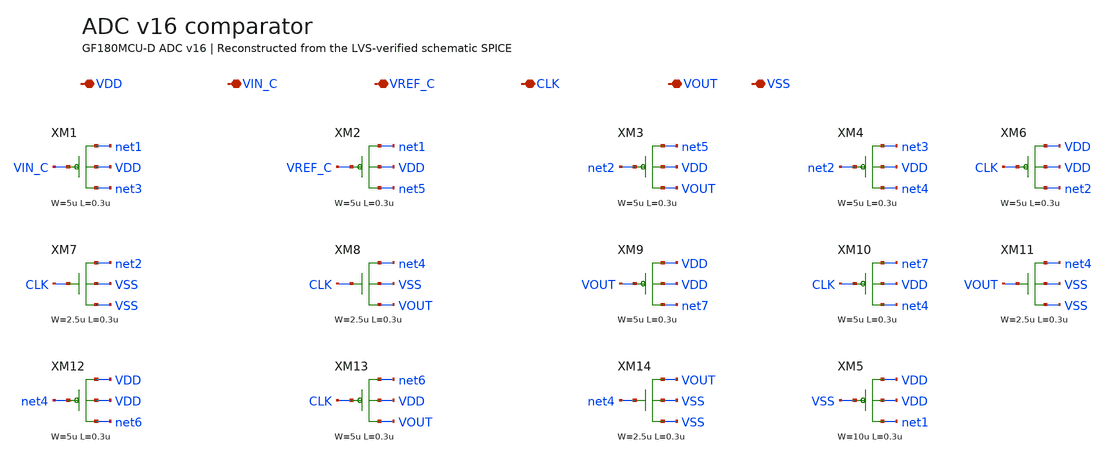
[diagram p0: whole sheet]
** sch_path: src/schematics/INTEGRATION/ADC_final/ADC_v17_Xschem/ADCv16_verified_comparator.sch
* Copyright (C) 1998-2026 Stefan Frederik Schippers
* This program is free software; you can redistribute it and/or modify
* it under the terms of the GNU General Public License as published by
* the Free Software Foundation; either version 2 of the License, or
* (at your option) any later version.
**.subckt ADCv16_verified_comparator VDD VIN_C VREF_C CLK VOUT VSS
*.iopin VDD
*.iopin VIN_C
*.iopin VREF_C
*.iopin CLK
*.iopin VOUT
*.iopin VSS
XM1 net3 VIN_C net1 VDD pfet_03v3 L=0.3u W=5u nf=1 ad='int((nf+1)/2) * W/nf * 0.18u' as='int((nf+2)/2) * W/nf * 0.18u'
+ pd='2*int((nf+1)/2) * (W/nf + 0.18u)' ps='2*int((nf+2)/2) * (W/nf + 0.18u)' nrd='0.18u / W' nrs='0.18u / W'
+ sa=0 sb=0 sd=0
XM2 net5 VREF_C net1 VDD pfet_03v3 L=0.3u W=5u nf=1 ad='int((nf+1)/2) * W/nf * 0.18u' as='int((nf+2)/2) * W/nf * 0.18u'
+ pd='2*int((nf+1)/2) * (W/nf + 0.18u)' ps='2*int((nf+2)/2) * (W/nf + 0.18u)' nrd='0.18u / W' nrs='0.18u / W'
+ sa=0 sb=0 sd=0
XM3 VOUT net2 net5 VDD pfet_03v3 L=0.3u W=5u nf=1 ad='int((nf+1)/2) * W/nf * 0.18u' as='int((nf+2)/2) * W/nf * 0.18u'
+ pd='2*int((nf+1)/2) * (W/nf + 0.18u)' ps='2*int((nf+2)/2) * (W/nf + 0.18u)' nrd='0.18u / W' nrs='0.18u / W'
+ sa=0 sb=0 sd=0
XM4 net4 net2 net3 VDD pfet_03v3 L=0.3u W=5u nf=1 ad='int((nf+1)/2) * W/nf * 0.18u' as='int((nf+2)/2) * W/nf * 0.18u'
+ pd='2*int((nf+1)/2) * (W/nf + 0.18u)' ps='2*int((nf+2)/2) * (W/nf + 0.18u)' nrd='0.18u / W' nrs='0.18u / W'
+ sa=0 sb=0 sd=0
XM6 net2 CLK VDD VDD pfet_03v3 L=0.3u W=5u nf=1 ad='int((nf+1)/2) * W/nf * 0.18u' as='int((nf+2)/2) * W/nf * 0.18u'
+ pd='2*int((nf+1)/2) * (W/nf + 0.18u)' ps='2*int((nf+2)/2) * (W/nf + 0.18u)' nrd='0.18u / W' nrs='0.18u / W'
+ sa=0 sb=0 sd=0
XM7 net2 CLK VSS VSS nfet_03v3 L=0.3u W=2.5u nf=1 ad='int((nf+1)/2) * W/nf * 0.18u' as='int((nf+2)/2) * W/nf * 0.18u'
+ pd='2*int((nf+1)/2) * (W/nf + 0.18u)' ps='2*int((nf+2)/2) * (W/nf + 0.18u)' nrd='0.18u / W' nrs='0.18u / W'
+ sa=0 sb=0 sd=0
XM8 net4 CLK VOUT VSS nfet_03v3 L=0.3u W=2.5u nf=1 ad='int((nf+1)/2) * W/nf * 0.18u' as='int((nf+2)/2) * W/nf * 0.18u'
+ pd='2*int((nf+1)/2) * (W/nf + 0.18u)' ps='2*int((nf+2)/2) * (W/nf + 0.18u)' nrd='0.18u / W' nrs='0.18u / W'
+ sa=0 sb=0 sd=0
XM9 net7 VOUT VDD VDD pfet_03v3 L=0.3u W=5u nf=1 ad='int((nf+1)/2) * W/nf * 0.18u' as='int((nf+2)/2) * W/nf * 0.18u'
+ pd='2*int((nf+1)/2) * (W/nf + 0.18u)' ps='2*int((nf+2)/2) * (W/nf + 0.18u)' nrd='0.18u / W' nrs='0.18u / W'
+ sa=0 sb=0 sd=0
XM10 net4 CLK net7 VDD pfet_03v3 L=0.3u W=5u nf=1 ad='int((nf+1)/2) * W/nf * 0.18u' as='int((nf+2)/2) * W/nf * 0.18u'
+ pd='2*int((nf+1)/2) * (W/nf + 0.18u)' ps='2*int((nf+2)/2) * (W/nf + 0.18u)' nrd='0.18u / W' nrs='0.18u / W'
+ sa=0 sb=0 sd=0
XM11 net4 VOUT VSS VSS nfet_03v3 L=0.3u W=2.5u nf=1 ad='int((nf+1)/2) * W/nf * 0.18u' as='int((nf+2)/2) * W/nf * 0.18u'
+ pd='2*int((nf+1)/2) * (W/nf + 0.18u)' ps='2*int((nf+2)/2) * (W/nf + 0.18u)' nrd='0.18u / W' nrs='0.18u / W'
+ sa=0 sb=0 sd=0
XM12 net6 net4 VDD VDD pfet_03v3 L=0.3u W=5u nf=1 ad='int((nf+1)/2) * W/nf * 0.18u' as='int((nf+2)/2) * W/nf * 0.18u'
+ pd='2*int((nf+1)/2) * (W/nf + 0.18u)' ps='2*int((nf+2)/2) * (W/nf + 0.18u)' nrd='0.18u / W' nrs='0.18u / W'
+ sa=0 sb=0 sd=0
XM13 VOUT CLK net6 VDD pfet_03v3 L=0.3u W=5u nf=1 ad='int((nf+1)/2) * W/nf * 0.18u' as='int((nf+2)/2) * W/nf * 0.18u'
+ pd='2*int((nf+1)/2) * (W/nf + 0.18u)' ps='2*int((nf+2)/2) * (W/nf + 0.18u)' nrd='0.18u / W' nrs='0.18u / W'
+ sa=0 sb=0 sd=0
XM14 VOUT net4 VSS VSS nfet_03v3 L=0.3u W=2.5u nf=1 ad='int((nf+1)/2) * W/nf * 0.18u' as='int((nf+2)/2) * W/nf * 0.18u'
+ pd='2*int((nf+1)/2) * (W/nf + 0.18u)' ps='2*int((nf+2)/2) * (W/nf + 0.18u)' nrd='0.18u / W' nrs='0.18u / W'
+ sa=0 sb=0 sd=0
XM5 net1 VSS VDD VDD pfet_03v3 L=0.3u W=10u nf=1 ad='int((nf+1)/2) * W/nf * 0.18u' as='int((nf+2)/2) * W/nf * 0.18u'
+ pd='2*int((nf+1)/2) * (W/nf + 0.18u)' ps='2*int((nf+2)/2) * (W/nf + 0.18u)' nrd='0.18u / W' nrs='0.18u / W'
+ sa=0 sb=0 sd=0
**.ends
.end
